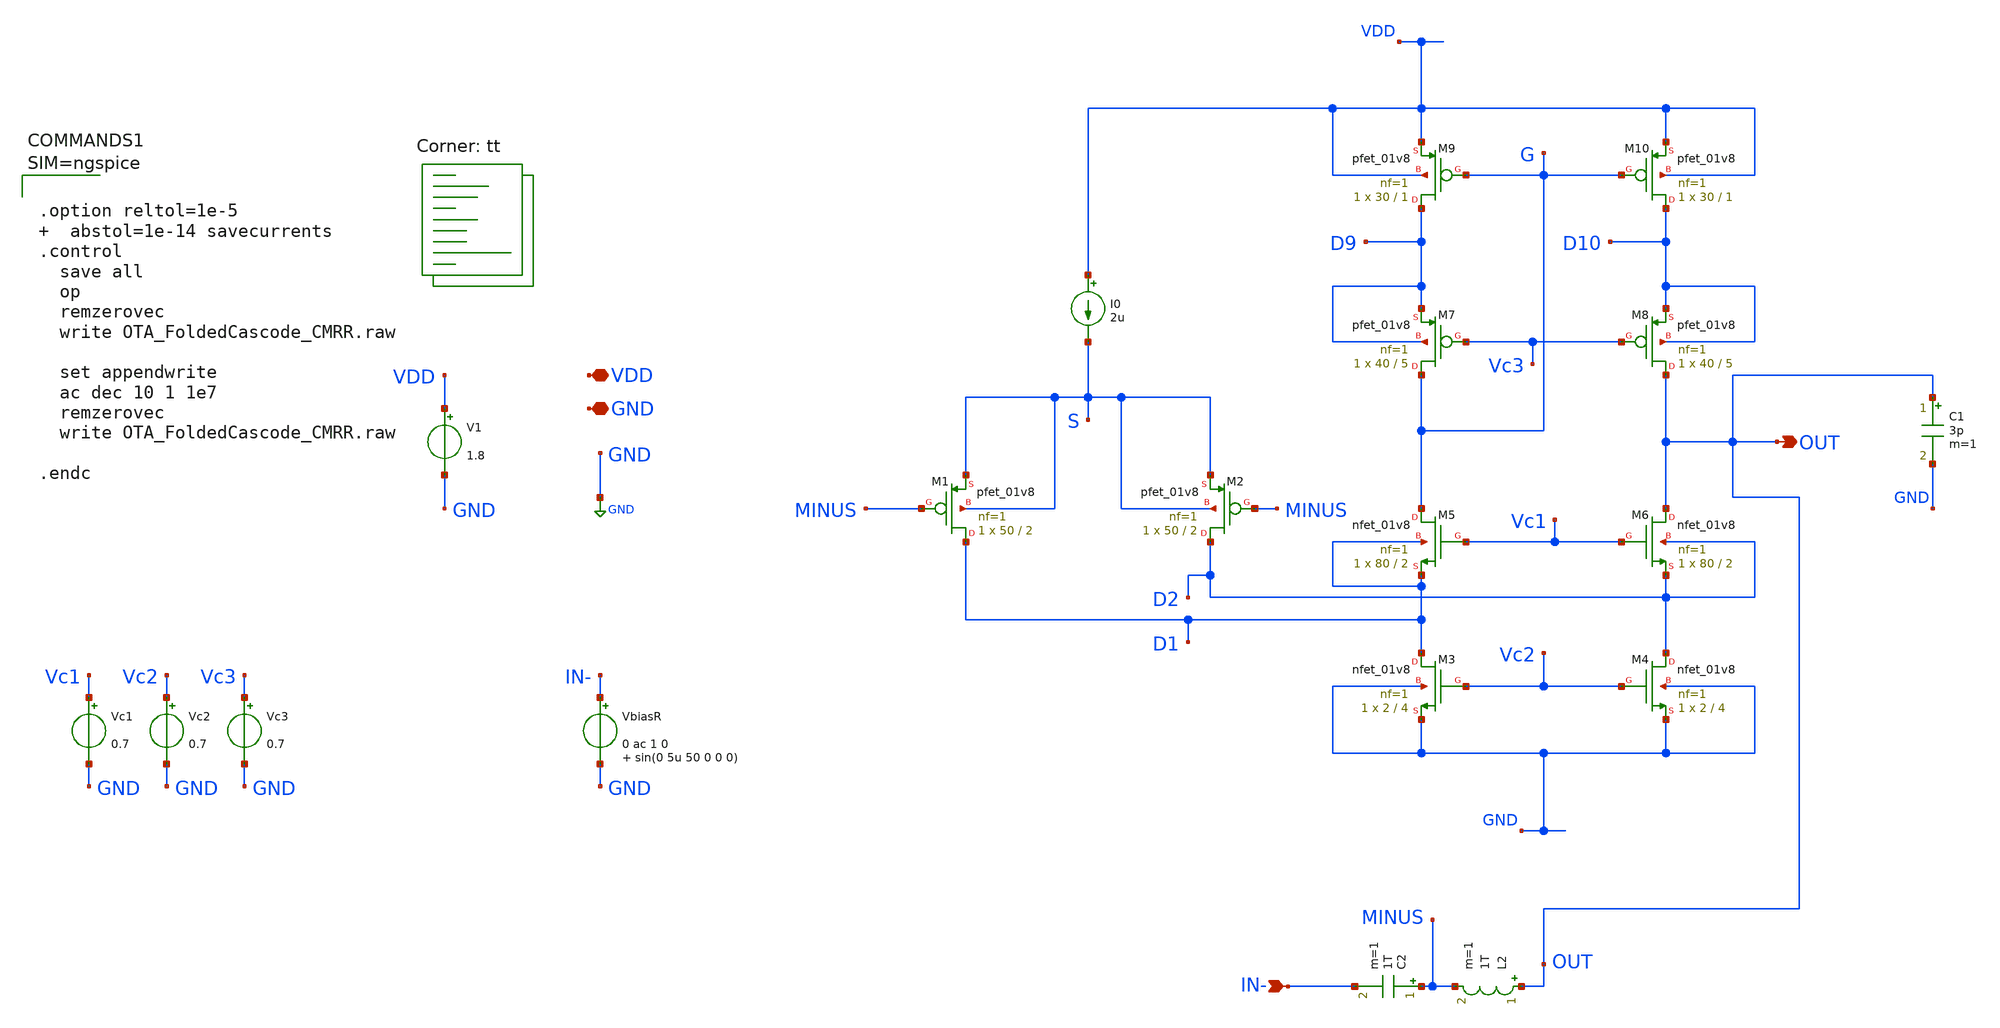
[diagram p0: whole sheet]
** sch_path: xschem/OTA_FoldedCascode_CMRR.sch
**.subckt OTA_FoldedCascode_CMRR VDD GND IN- OUT
*.iopin VDD
*.iopin GND
*.ipin IN-
*.opin OUT
V1 VDD GND 1.8
VbiasR IN- GND 0 ac 1 0 sin(0 5u 50 0 0 0)
I0 VDD S 2u
XM1 D1 MINUS S S sky130_fd_pr__pfet_01v8 L=2 W=50 nf=1 ad='int((nf+1)/2) * W/nf * 0.29' as='int((nf+2)/2) * W/nf * 0.29'
+ pd='2*int((nf+1)/2) * (W/nf + 0.29)' ps='2*int((nf+2)/2) * (W/nf + 0.29)' nrd='0.29 / W' nrs='0.29 / W'
+ sa=0 sb=0 sd=0 mult=1 m=1
XM2 D2 MINUS S S sky130_fd_pr__pfet_01v8 L=2 W=50 nf=1 ad='int((nf+1)/2) * W/nf * 0.29' as='int((nf+2)/2) * W/nf * 0.29'
+ pd='2*int((nf+1)/2) * (W/nf + 0.29)' ps='2*int((nf+2)/2) * (W/nf + 0.29)' nrd='0.29 / W' nrs='0.29 / W'
+ sa=0 sb=0 sd=0 mult=1 m=1
XM3 D1 Vc2 GND GND sky130_fd_pr__nfet_01v8 L=4 W=2 nf=1 ad='int((nf+1)/2) * W/nf * 0.29' as='int((nf+2)/2) * W/nf * 0.29'
+ pd='2*int((nf+1)/2) * (W/nf + 0.29)' ps='2*int((nf+2)/2) * (W/nf + 0.29)' nrd='0.29 / W' nrs='0.29 / W'
+ sa=0 sb=0 sd=0 mult=1 m=1
XM4 D2 Vc2 GND GND sky130_fd_pr__nfet_01v8 L=4 W=2 nf=1 ad='int((nf+1)/2) * W/nf * 0.29' as='int((nf+2)/2) * W/nf * 0.29'
+ pd='2*int((nf+1)/2) * (W/nf + 0.29)' ps='2*int((nf+2)/2) * (W/nf + 0.29)' nrd='0.29 / W' nrs='0.29 / W'
+ sa=0 sb=0 sd=0 mult=1 m=1
XM5 G Vc1 D1 D1 sky130_fd_pr__nfet_01v8 L=2 W=80 nf=1 ad='int((nf+1)/2) * W/nf * 0.29' as='int((nf+2)/2) * W/nf * 0.29'
+ pd='2*int((nf+1)/2) * (W/nf + 0.29)' ps='2*int((nf+2)/2) * (W/nf + 0.29)' nrd='0.29 / W' nrs='0.29 / W'
+ sa=0 sb=0 sd=0 mult=1 m=1
XM6 OUT Vc1 D2 D2 sky130_fd_pr__nfet_01v8 L=2 W=80 nf=1 ad='int((nf+1)/2) * W/nf * 0.29' as='int((nf+2)/2) * W/nf * 0.29'
+ pd='2*int((nf+1)/2) * (W/nf + 0.29)' ps='2*int((nf+2)/2) * (W/nf + 0.29)' nrd='0.29 / W' nrs='0.29 / W'
+ sa=0 sb=0 sd=0 mult=1 m=1
XM7 G Vc3 D9 D9 sky130_fd_pr__pfet_01v8 L=5 W=40 nf=1 ad='int((nf+1)/2) * W/nf * 0.29' as='int((nf+2)/2) * W/nf * 0.29'
+ pd='2*int((nf+1)/2) * (W/nf + 0.29)' ps='2*int((nf+2)/2) * (W/nf + 0.29)' nrd='0.29 / W' nrs='0.29 / W'
+ sa=0 sb=0 sd=0 mult=1 m=1
XM8 OUT Vc3 D10 D10 sky130_fd_pr__pfet_01v8 L=5 W=40 nf=1 ad='int((nf+1)/2) * W/nf * 0.29' as='int((nf+2)/2) * W/nf * 0.29'
+ pd='2*int((nf+1)/2) * (W/nf + 0.29)' ps='2*int((nf+2)/2) * (W/nf + 0.29)' nrd='0.29 / W' nrs='0.29 / W'
+ sa=0 sb=0 sd=0 mult=1 m=1
XM9 D9 G VDD VDD sky130_fd_pr__pfet_01v8 L=1 W=30 nf=1 ad='int((nf+1)/2) * W/nf * 0.29' as='int((nf+2)/2) * W/nf * 0.29'
+ pd='2*int((nf+1)/2) * (W/nf + 0.29)' ps='2*int((nf+2)/2) * (W/nf + 0.29)' nrd='0.29 / W' nrs='0.29 / W'
+ sa=0 sb=0 sd=0 mult=1 m=1
XM10 D10 G VDD VDD sky130_fd_pr__pfet_01v8 L=1 W=30 nf=1 ad='int((nf+1)/2) * W/nf * 0.29' as='int((nf+2)/2) * W/nf * 0.29'
+ pd='2*int((nf+1)/2) * (W/nf + 0.29)' ps='2*int((nf+2)/2) * (W/nf + 0.29)' nrd='0.29 / W' nrs='0.29 / W'
+ sa=0 sb=0 sd=0 mult=1 m=1
Vc1 Vc1 GND 0.7
Vc2 Vc2 GND 0.7
Vc3 Vc3 GND 0.7
C2 MINUS IN- 1T m=1
L2 OUT MINUS 1T m=1
C1 OUT GND 3p m=1
**** begin user architecture code



.option reltol=1e-5   abstol=1e-14 savecurrents
.control
  save all
  op
  remzerovec
  write OTA_FoldedCascode_CMRR.raw

  set appendwrite
  ac dec 10 1 1e7
  remzerovec
  write OTA_FoldedCascode_CMRR.raw

.endc



.lib $::SKYWATER_MODELS/sky130.lib.spice tt
**** end user architecture code
**.ends
.GLOBAL GND
.end
